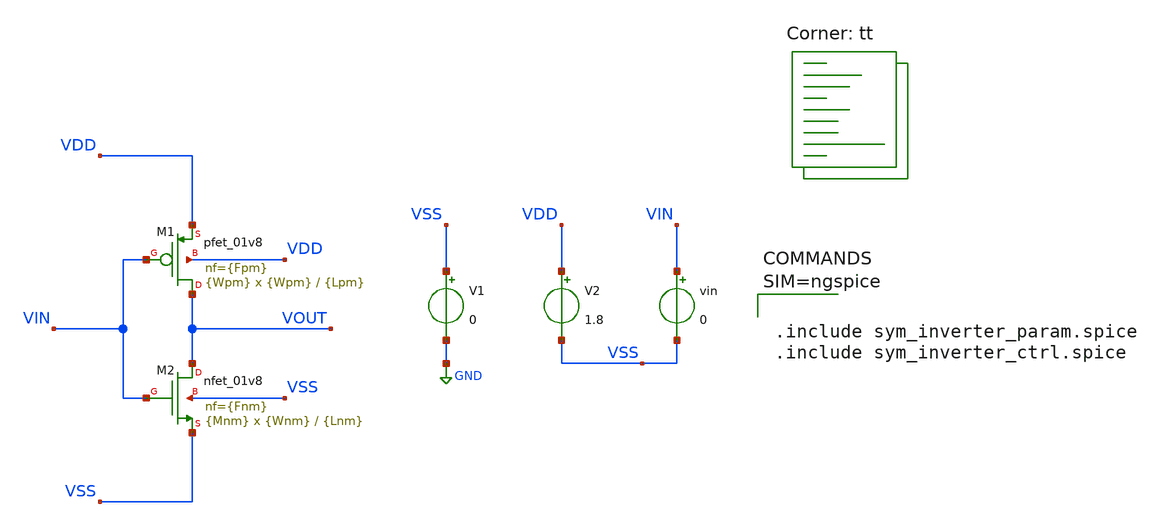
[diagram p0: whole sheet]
** sch_path: work/design/sym_inverter.sch
**.subckt sym_inverter
V1 VSS GND 0
V2 VDD VSS 1.8
vin VIN VSS 0
XM2 VOUT VIN VSS VSS sky130_fd_pr__nfet_01v8 L={Lnm} W={Wnm} nf={Fnm} ad='int((nf+1)/2) * W/nf * 0.29'
+ as='int((nf+2)/2) * W/nf * 0.29' pd='2*int((nf+1)/2) * (W/nf + 0.29)' ps='2*int((nf+2)/2) * (W/nf + 0.29)'
+ nrd='0.29 / W' nrs='0.29 / W' sa=0 sb=0 sd=0 mult={Mnm} m={Mnm}
XM1 VOUT VIN VDD VDD sky130_fd_pr__pfet_01v8 L={Lpm} W={Wpm} nf={Fpm} ad='int((nf+1)/2) * W/nf * 0.29'
+ as='int((nf+2)/2) * W/nf * 0.29' pd='2*int((nf+1)/2) * (W/nf + 0.29)' ps='2*int((nf+2)/2) * (W/nf + 0.29)'
+ nrd='0.29 / W' nrs='0.29 / W' sa=0 sb=0 sd=0 mult={Wpm} m={Wpm}
**** begin user architecture code
.lib $::SKYWATER_MODELS/sky130.lib.spice tt



.include sym_inverter_param.spice
.include sym_inverter_ctrl.spice



**** end user architecture code
**.ends
.GLOBAL GND
.end
